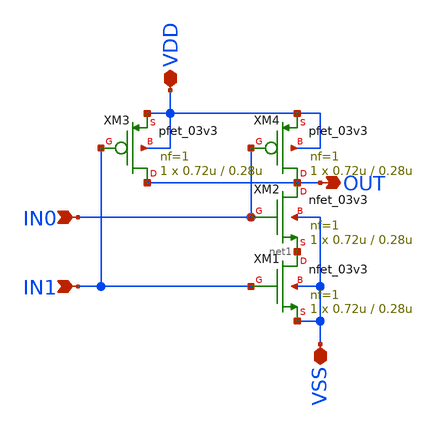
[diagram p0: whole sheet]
** sch_path: CAD7/datapath_nand2.sch
**.subckt datapath_nand2 VSS VDD IN0 IN1 OUT
*.iopin VSS
*.iopin VDD
*.ipin IN0
*.ipin IN1
*.opin OUT
XM1 net1 IN1 VSS VSS nfet_03v3 L=0.28u W=0.72u nf=1 ad='int((nf+1)/2) * W/nf * 0.18u' as='int((nf+2)/2) * W/nf * 0.18u'
+ pd='2*int((nf+1)/2) * (W/nf + 0.18u)' ps='2*int((nf+2)/2) * (W/nf + 0.18u)' nrd='0.18u / W' nrs='0.18u / W'
+ sa=0 sb=0 sd=0 m=1
XM2 OUT IN0 net1 VSS nfet_03v3 L=0.28u W=0.72u nf=1 ad='int((nf+1)/2) * W/nf * 0.18u' as='int((nf+2)/2) * W/nf * 0.18u'
+ pd='2*int((nf+1)/2) * (W/nf + 0.18u)' ps='2*int((nf+2)/2) * (W/nf + 0.18u)' nrd='0.18u / W' nrs='0.18u / W'
+ sa=0 sb=0 sd=0 m=1
XM3 OUT IN1 VDD VDD pfet_03v3 L=0.28u W=0.72u nf=1 ad='int((nf+1)/2) * W/nf * 0.18u' as='int((nf+2)/2) * W/nf * 0.18u'
+ pd='2*int((nf+1)/2) * (W/nf + 0.18u)' ps='2*int((nf+2)/2) * (W/nf + 0.18u)' nrd='0.18u / W' nrs='0.18u / W'
+ sa=0 sb=0 sd=0 m=1
XM4 OUT IN0 VDD VDD pfet_03v3 L=0.28u W=0.72u nf=1 ad='int((nf+1)/2) * W/nf * 0.18u' as='int((nf+2)/2) * W/nf * 0.18u'
+ pd='2*int((nf+1)/2) * (W/nf + 0.18u)' ps='2*int((nf+2)/2) * (W/nf + 0.18u)' nrd='0.18u / W' nrs='0.18u / W'
+ sa=0 sb=0 sd=0 m=1
**.ends
.end
